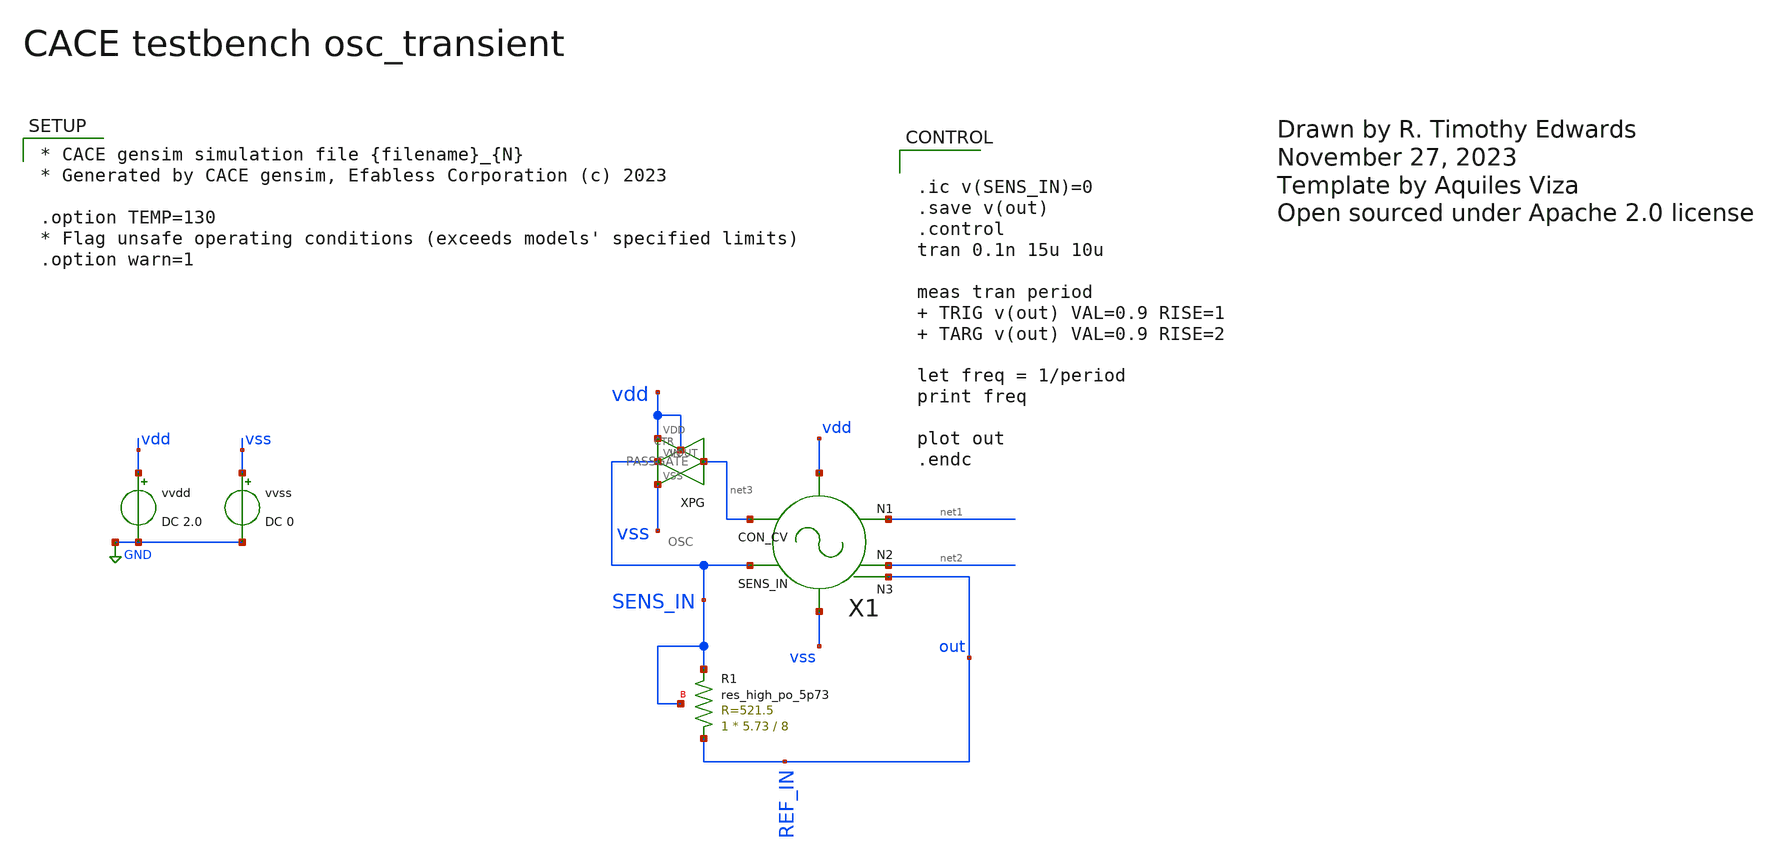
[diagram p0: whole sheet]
** sch_path: modules/OSC/test/transient.sch
* Open sourced under Apache 2.0 license

* CACE gensim simulation file {filename}_{N}
* Generated by CACE gensim, Efabless Corporation (c) 2023

.option TEMP=130
* Flag unsafe operating conditions (exceeds models' specified limits)
.option warn=1


**.subckt transient
vvss vss GND DC 0
vvdd vdd GND DC 2.0
X1 SENS_IN net1 net2 vdd vss net3 out OSC
XR1 out SENS_IN SENS_IN sky130_fd_pr__res_high_po_5p73 L=8 mult=1 m=1
XPG SENS_IN vdd net3 vdd vss PASSGATE
**** begin user architecture code


.ic v(SENS_IN)=0
.save v(out)
.control
tran 0.1n 15u 10u

meas tran period  TRIG v(out) VAL=0.9 RISE=1  TARG v(out) VAL=0.9 RISE=2

let freq = 1/period
print freq

plot out
.endc



*.lib $env(PDK_ROOT)/$env(PDK)/libs.tech/combined/sky130.lib.spice tt
.lib $env(PDK_ROOT)/$env(PDK)/libs.tech/ngspice/sky130.lib.spice.tt.red tt

.include $env(PDK_ROOT)/$env(PDK)/libs.ref/sky130_fd_sc_hd/spice/sky130_fd_sc_hd.spice

**** end user architecture code
**.ends
.GLOBAL GND
.end
